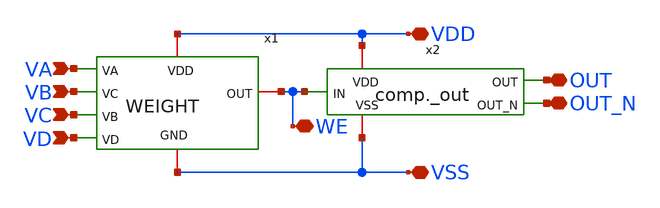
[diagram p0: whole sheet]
** sch_path: FINAL/XSCHEM/WEIGTH/WEIGHT_COMP.sch
**.subckt WEIGHT_COMP VDD VSS VA VB VC VD WE OUT OUT_N
*.iopin VDD
*.iopin VSS
*.ipin VA
*.ipin VB
*.ipin VC
*.ipin VD
*.iopin WE
*.iopin OUT
*.iopin OUT_N
x1 VDD VSS WE VA VB VC VD WEIGHT
x2 VDD OUT WE OUT_N VSS comp._out
**.ends
.end
